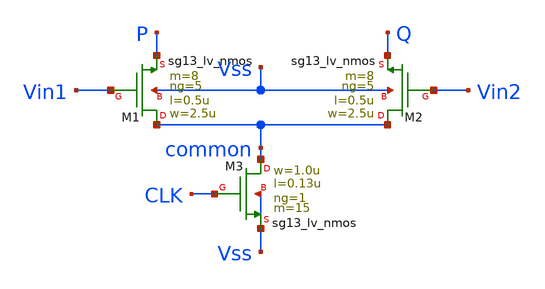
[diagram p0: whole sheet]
** sch_path: klayout/LVS/SA_lower.sch
**.subckt SA_lower
XM1 common Vin1 P Vss sg13_lv_nmos w=2.5u l=0.5u ng=5 m=8 mm_ok=1
XM3 common CLK Vss Vss sg13_lv_nmos w=1.0u l=0.13u ng=1 m=15 mm_ok=1
XM2 common Vin2 Q Vss sg13_lv_nmos w=2.5u l=0.5u ng=5 m=8 mm_ok=1
**.ends
.end
